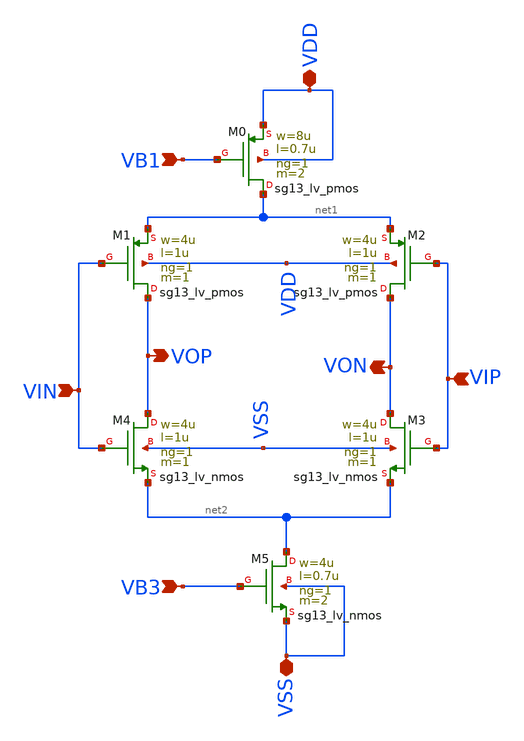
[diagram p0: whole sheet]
** sch_path: AMP_INV_08V.sch
**.subckt AMP_INV_08V VDD VSS VOP VON VIN VIP VB3 VB1
*.iopin VDD
*.iopin VSS
*.opin VOP
*.opin VON
*.ipin VIN
*.ipin VIP
*.ipin VB3
*.ipin VB1
XM4 VOP VIN net2 VSS sg13_lv_nmos w=4u l=1u ng=1 m=1 mm_ok=1
XM0 net1 VB1 VDD VDD sg13_lv_pmos w=8u l=0.7u ng=1 m=2 mm_ok=1
XM5 net2 VB3 VSS VSS sg13_lv_nmos w=4u l=0.7u ng=1 m=2 mm_ok=1
XM3 VON VIP net2 VSS sg13_lv_nmos w=4u l=1u ng=1 m=1 mm_ok=1
XM2 VON VIP net1 VDD sg13_lv_pmos w=4u l=1u ng=1 m=1 mm_ok=1
XM1 VOP VIN net1 VDD sg13_lv_pmos w=4u l=1u ng=1 m=1 mm_ok=1
**.ends
.end
